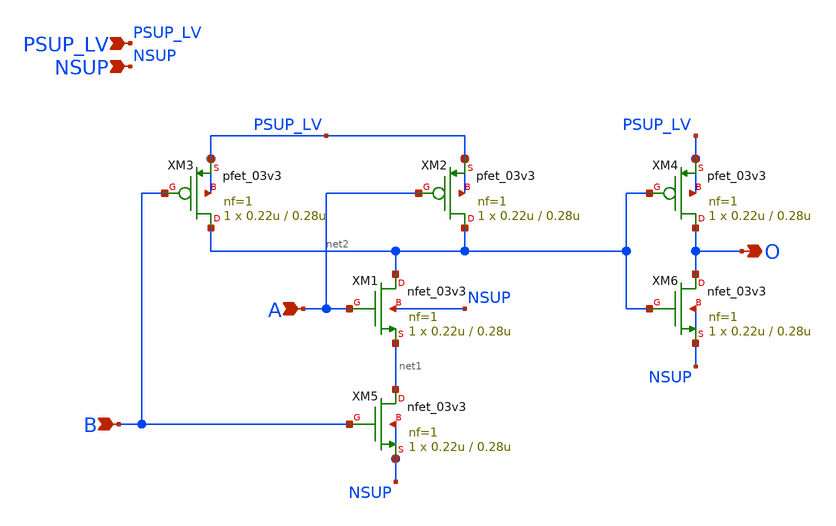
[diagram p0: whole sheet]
** sch_path: xschem/blocks/and/and.sch
**.subckt and PSUP_LV NSUP A B O
*.ipin PSUP_LV
*.ipin NSUP
*.ipin A
*.ipin B
*.opin O
XM5 net1 B NSUP NSUP nfet_03v3 L=0.28u W=0.22u nf=1 ad='int((nf+1)/2) * W/nf * 0.18u' as='int((nf+2)/2) * W/nf * 0.18u'
+ pd='2*int((nf+1)/2) * (W/nf + 0.18u)' ps='2*int((nf+2)/2) * (W/nf + 0.18u)' nrd='0.18u / W' nrs='0.18u / W'
+ sa=0 sb=0 sd=0 m=1
XM1 net2 A net1 NSUP nfet_03v3 L=0.28u W=0.22u nf=1 ad='int((nf+1)/2) * W/nf * 0.18u' as='int((nf+2)/2) * W/nf * 0.18u'
+ pd='2*int((nf+1)/2) * (W/nf + 0.18u)' ps='2*int((nf+2)/2) * (W/nf + 0.18u)' nrd='0.18u / W' nrs='0.18u / W'
+ sa=0 sb=0 sd=0 m=1
XM2 net2 A PSUP_LV PSUP_LV pfet_03v3 L=0.28u W=0.22u nf=1 ad='int((nf+1)/2) * W/nf * 0.18u' as='int((nf+2)/2) * W/nf * 0.18u'
+ pd='2*int((nf+1)/2) * (W/nf + 0.18u)' ps='2*int((nf+2)/2) * (W/nf + 0.18u)' nrd='0.18u / W' nrs='0.18u / W'
+ sa=0 sb=0 sd=0 m=1
XM3 net2 B PSUP_LV PSUP_LV pfet_03v3 L=0.28u W=0.22u nf=1 ad='int((nf+1)/2) * W/nf * 0.18u' as='int((nf+2)/2) * W/nf * 0.18u'
+ pd='2*int((nf+1)/2) * (W/nf + 0.18u)' ps='2*int((nf+2)/2) * (W/nf + 0.18u)' nrd='0.18u / W' nrs='0.18u / W'
+ sa=0 sb=0 sd=0 m=1
XM4 O net2 PSUP_LV PSUP_LV pfet_03v3 L=0.28u W=0.22u nf=1 ad='int((nf+1)/2) * W/nf * 0.18u' as='int((nf+2)/2) * W/nf * 0.18u'
+ pd='2*int((nf+1)/2) * (W/nf + 0.18u)' ps='2*int((nf+2)/2) * (W/nf + 0.18u)' nrd='0.18u / W' nrs='0.18u / W'
+ sa=0 sb=0 sd=0 m=1
XM6 O net2 NSUP NSUP nfet_03v3 L=0.28u W=0.22u nf=1 ad='int((nf+1)/2) * W/nf * 0.18u' as='int((nf+2)/2) * W/nf * 0.18u'
+ pd='2*int((nf+1)/2) * (W/nf + 0.18u)' ps='2*int((nf+2)/2) * (W/nf + 0.18u)' nrd='0.18u / W' nrs='0.18u / W'
+ sa=0 sb=0 sd=0 m=1
**.ends
.end
